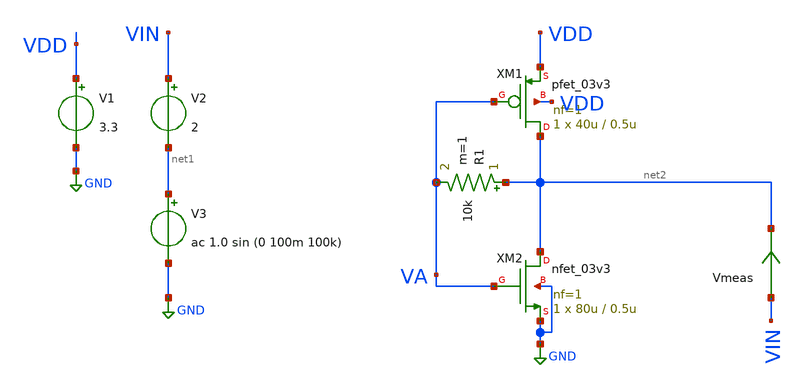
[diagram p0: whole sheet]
** sch_path: output_impedance/output_impedance7.sch
**.subckt output_impedance7
V1 VDD GND 3.3
V2 VIN net1 2
Vmeas VIN net2 0
.save i(vmeas)
V3 net1 GND ac 1.0 sin (0 100m 100k)
XM2 net2 VA GND GND nfet_03v3 L=0.5u W=80u nf=1 ad='int((nf+1)/2) * W/nf * 0.18u' as='int((nf+2)/2) * W/nf * 0.18u'
+ pd='2*int((nf+1)/2) * (W/nf + 0.18u)' ps='2*int((nf+2)/2) * (W/nf + 0.18u)' nrd='0.18u / W' nrs='0.18u / W'
+ sa=0 sb=0 sd=0 m=1
XM1 net2 VA VDD VDD pfet_03v3 L=0.5u W=40u nf=1 ad='int((nf+1)/2) * W/nf * 0.18u' as='int((nf+2)/2) * W/nf * 0.18u'
+ pd='2*int((nf+1)/2) * (W/nf + 0.18u)' ps='2*int((nf+2)/2) * (W/nf + 0.18u)' nrd='0.18u / W' nrs='0.18u / W'
+ sa=0 sb=0 sd=0 m=1
R1 net2 VA 10k m=1
**** begin user architecture code

.include $::180MCU_MODELS/design.ngspice
*.lib $::180MCU_MODELS/sm141064.ngspice statistical
*.lib $::180MCU_MODELS/sm141064.ngspice res_statistical
.lib $::180MCU_MODELS/sm141064.ngspice typical
.lib $::180MCU_MODELS/sm141064.ngspice res_typical
.lib $::180MCU_MODELS/sm141064.ngspice moscap_typical
.lib $::180MCU_MODELS/sm141064.ngspice bjt_typical
.lib $::180MCU_MODELS/sm141064.ngspice diode_typical
.lib $::180MCU_MODELS/sm141064.ngspice mimcap_typical
.TEMP 27

.param   sw_stat_global = 1   sw_stat_mism = 1  mc_skew = 3  res_mc_skew = 3  cap_mc_skew = 3
+  fnoicor = 1



.control
save all
dc V2 0 3.3 0.01
plot v(Va)

plot i(Vmeas) 1/(deriv(i(Vmeas)))
plot i(Vmeas)
plot deriv(v(VOUT))
tran 100n 10u
plot i(Vmeas)
.endc

**** end user architecture code
**.ends
.GLOBAL GND
.end
